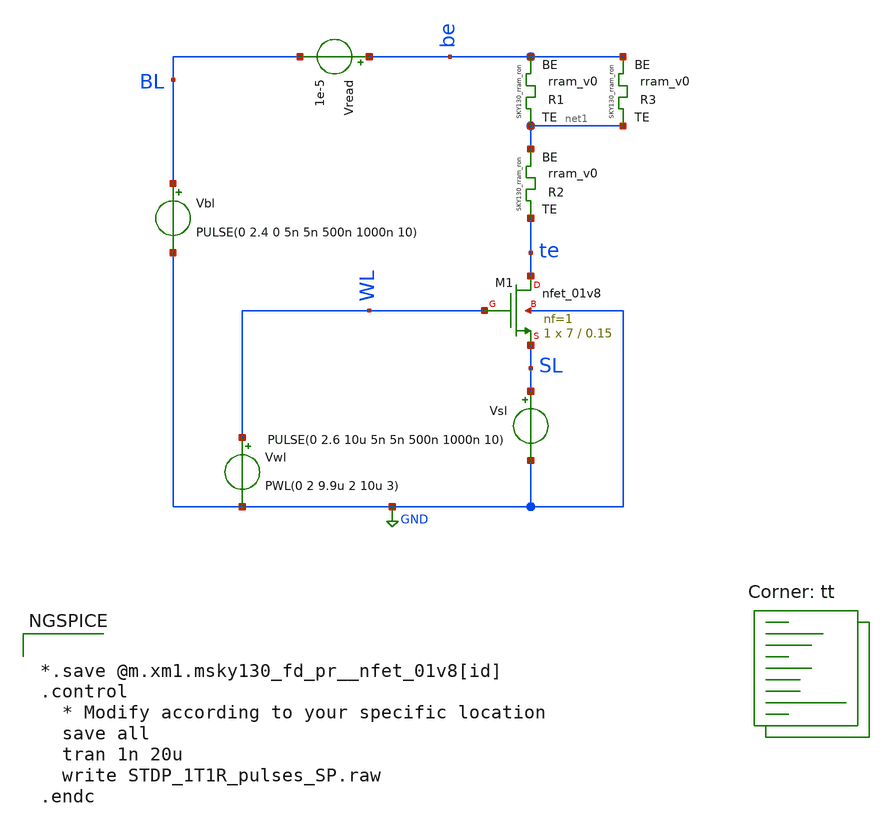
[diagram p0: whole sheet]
** sch_path: STDP_test/STDP_1T1R_pulses_SP.sch
**.subckt STDP_1T1R_pulses_SP
XM1 te WL SL GND sky130_fd_pr__nfet_01v8 L=0.15 W=7 nf=1 ad='int((nf+1)/2) * W/nf * 0.29' as='int((nf+2)/2) * W/nf * 0.29'
+ pd='2*int((nf+1)/2) * (W/nf + 0.29)' ps='2*int((nf+2)/2) * (W/nf + 0.29)' nrd='0.29 / W' nrs='0.29 / W'
+ sa=0 sb=0 sd=0 mult=1 m=1
Vwl WL GND PWL(0 2 9.9u 2 10u 3)
Vbl BL GND PULSE(0 2.4 0 5n 5n 500n 1000n 10)
Vread be BL 1e-5
XR1 net1 be rram_v0
Vsl SL GND PULSE(0 2.6 10u 5n 5n 500n 1000n 10)
XR2 te net1 rram_v0
XR3 net1 be rram_v0
**** begin user architecture code


*.save @m.xm1.msky130_fd_pr__nfet_01v8[id]
.control
  * Modify according to your specific location
  save all
  tran 1n 20u
  write STDP_1T1R_pulses_SP.raw
.endc



.lib $::SKYWATER_MODELS/sky130.lib.spice tt

** opencircuitdesign pdks install
.inc $::SKYWATER_MODELS/rram_v0.spice

**** end user architecture code
**.ends
.GLOBAL GND
.end
